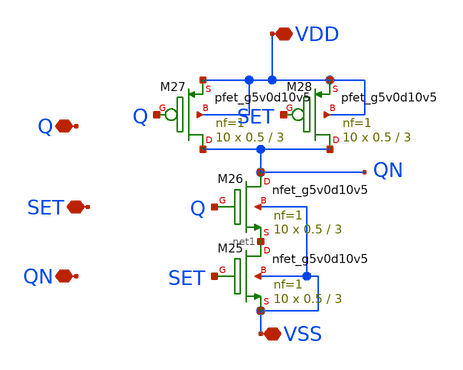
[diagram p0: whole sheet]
** sch_path: LS_boot_20230921/sch/NAND_5V.sch
**.subckt NAND_5V VSS VDD Q SET QN
*.iopin VSS
*.iopin VDD
*.iopin Q
*.iopin SET
*.iopin QN
XM25 net1 SET VSS VSS sky130_fd_pr__nfet_g5v0d10v5 L=3 W=0.5 nf=1 ad='int((nf+1)/2) * W/nf * 0.29' as='int((nf+2)/2) * W/nf * 0.29'
+ pd='2*int((nf+1)/2) * (W/nf + 0.29)' ps='2*int((nf+2)/2) * (W/nf + 0.29)' nrd='0.29 / W' nrs='0.29 / W'
+ sa=0 sb=0 sd=0 mult=10 m=10
XM26 QN Q net1 VSS sky130_fd_pr__nfet_g5v0d10v5 L=3 W=0.5 nf=1 ad='int((nf+1)/2) * W/nf * 0.29' as='int((nf+2)/2) * W/nf * 0.29'
+ pd='2*int((nf+1)/2) * (W/nf + 0.29)' ps='2*int((nf+2)/2) * (W/nf + 0.29)' nrd='0.29 / W' nrs='0.29 / W'
+ sa=0 sb=0 sd=0 mult=10 m=10
XM27 QN Q VDD VDD sky130_fd_pr__pfet_g5v0d10v5 L=3 W=0.5 nf=1 ad='int((nf+1)/2) * W/nf * 0.29' as='int((nf+2)/2) * W/nf * 0.29'
+ pd='2*int((nf+1)/2) * (W/nf + 0.29)' ps='2*int((nf+2)/2) * (W/nf + 0.29)' nrd='0.29 / W' nrs='0.29 / W'
+ sa=0 sb=0 sd=0 mult=10 m=10
XM28 QN SET VDD VDD sky130_fd_pr__pfet_g5v0d10v5 L=3 W=0.5 nf=1 ad='int((nf+1)/2) * W/nf * 0.29' as='int((nf+2)/2) * W/nf * 0.29'
+ pd='2*int((nf+1)/2) * (W/nf + 0.29)' ps='2*int((nf+2)/2) * (W/nf + 0.29)' nrd='0.29 / W' nrs='0.29 / W'
+ sa=0 sb=0 sd=0 mult=10 m=10
**.ends
.end
